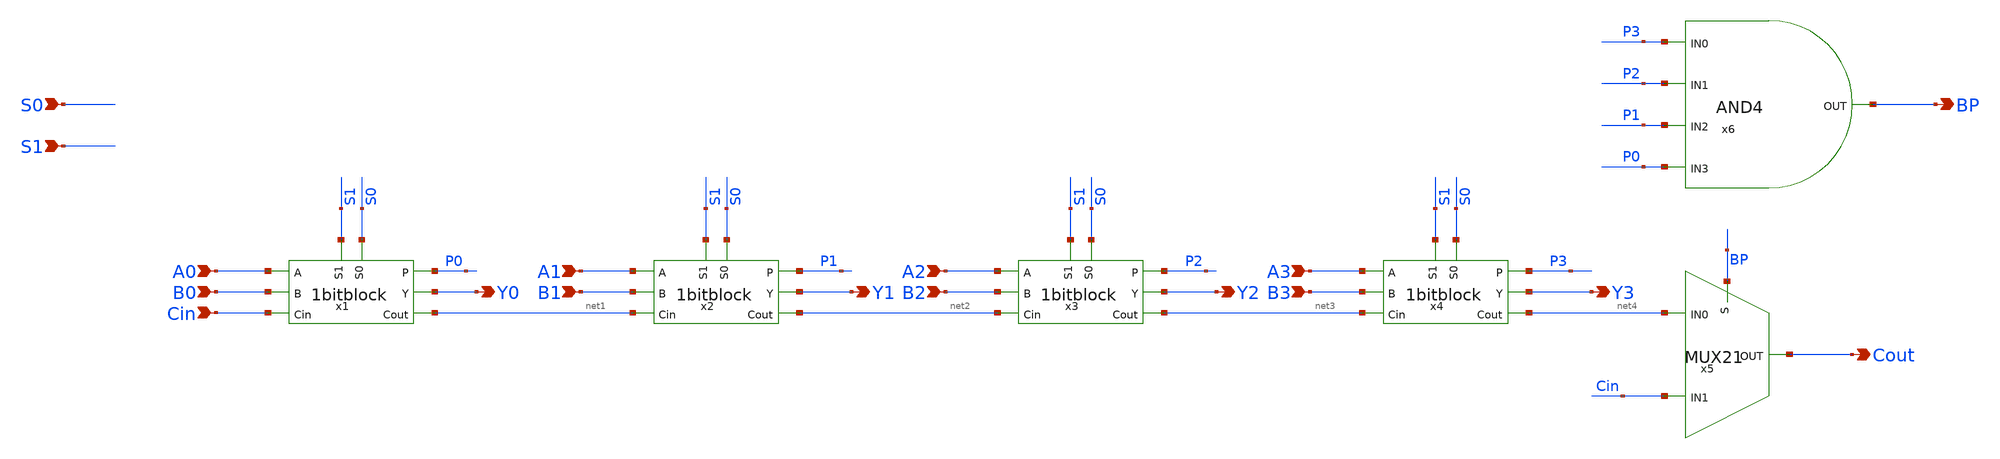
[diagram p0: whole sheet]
** sch_path: schematics/add/4bitblock.sch
**.subckt 4bitblock A0 B0 Cin S0 S1 Y0 A1 B1 A2 B2 A3 B3 Y1 Y2 Y3 Cout BP
*.ipin A0
*.ipin B0
*.ipin Cin
*.ipin S0
*.ipin S1
*.opin Y0
*.ipin A1
*.ipin B1
*.ipin A2
*.ipin B2
*.ipin A3
*.ipin B3
*.opin Y1
*.opin Y2
*.opin Y3
*.opin Cout
*.opin BP
x1 P0 A0 B0 Cin S0 S1 Y0 net1 1bitblock
x2 P1 A1 B1 net1 S0 S1 Y1 net2 1bitblock
x3 P2 A2 B2 net2 S0 S1 Y2 net3 1bitblock
x4 P3 A3 B3 net3 S0 S1 Y3 net4 1bitblock
x5 net4 BP Cout Cin MUX21
x6 BP P3 P2 P1 P0 AND4
**.ends
.end
